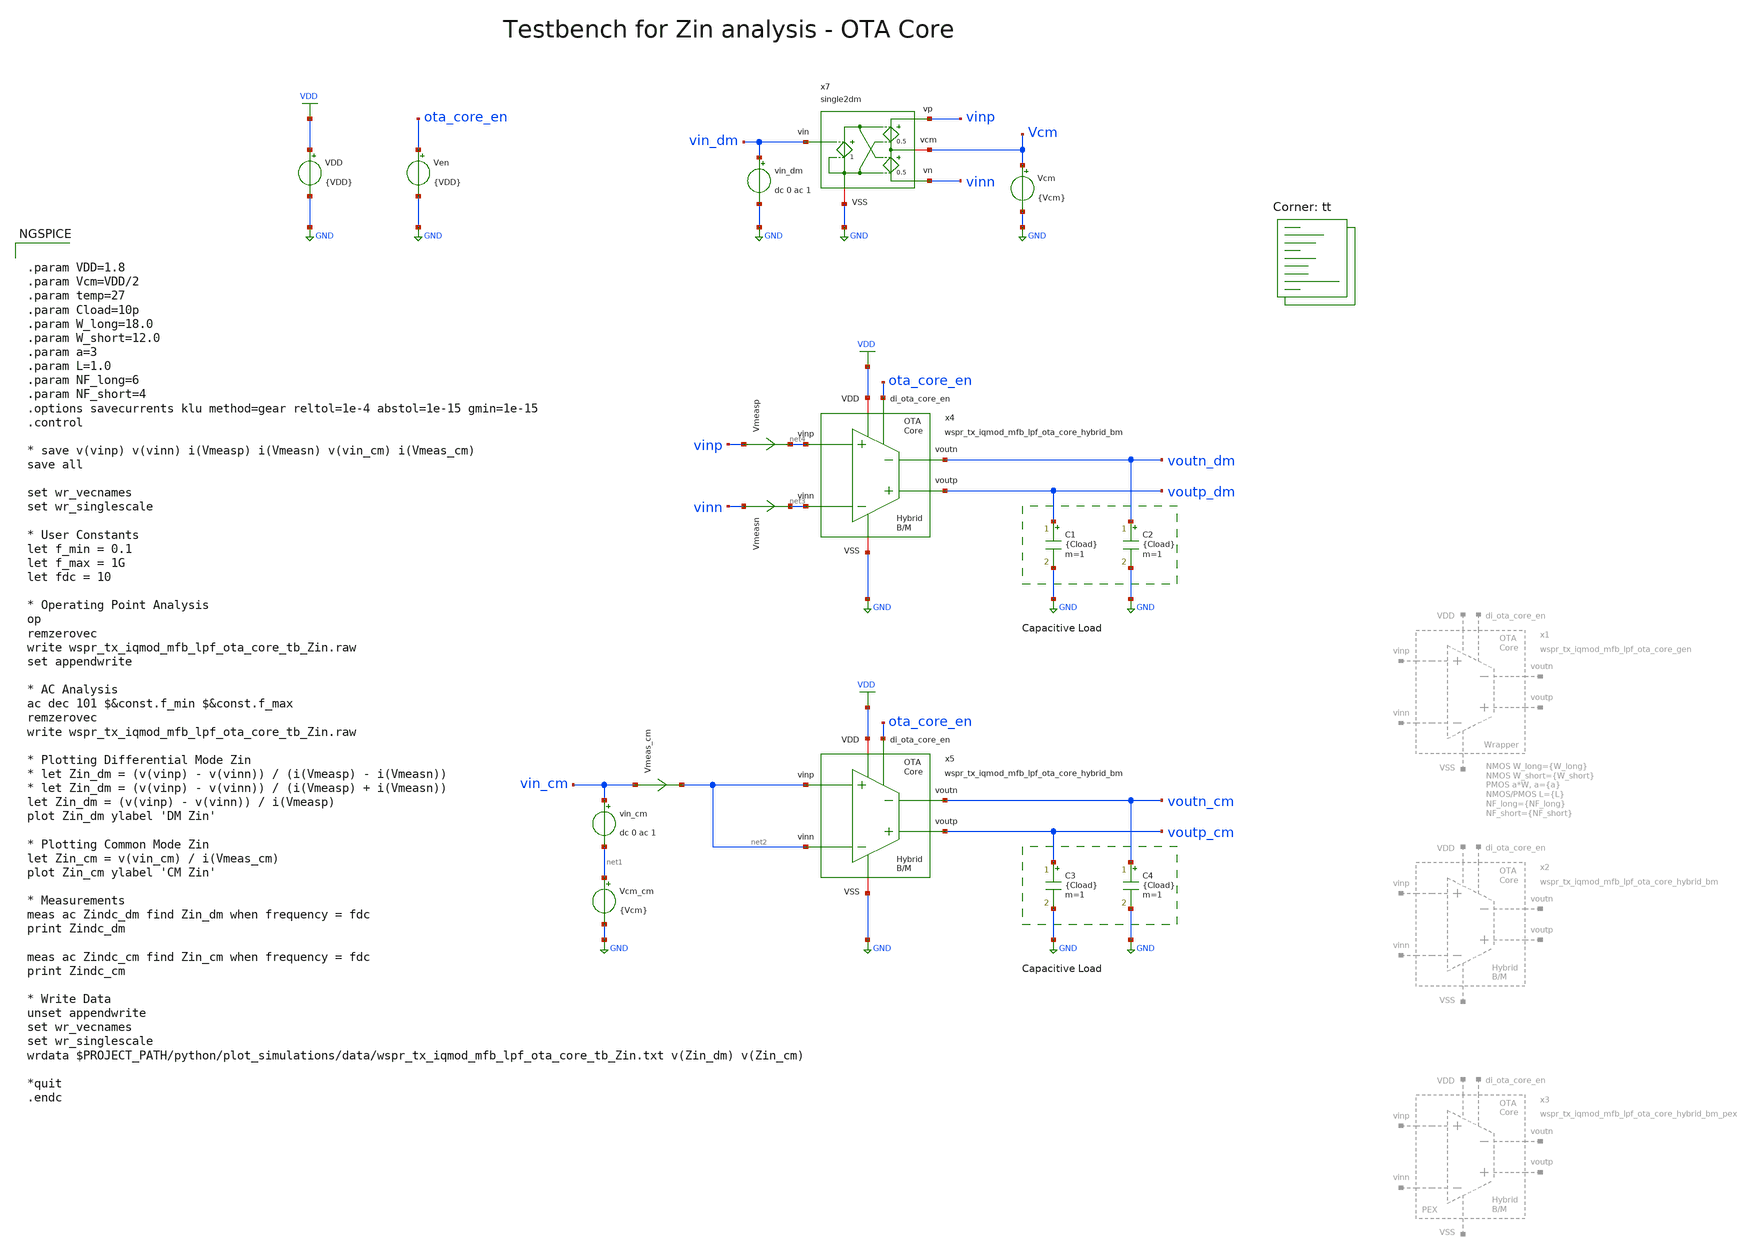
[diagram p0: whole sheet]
** sch_path: sky130/macros/iqmod/testbenches/wspr_tx_iqmod_mfb_lpf_ota_core_tb_Zin.sch
**.subckt wspr_tx_iqmod_mfb_lpf_ota_core_tb_Zin
VDD VDD GND {VDD}
C1 voutp_dm GND {Cload} m=1
C2 voutn_dm GND {Cload} m=1
Ven ota_core_en GND {VDD}
C3 voutp_cm GND {Cload} m=1
C4 voutn_cm GND {Cload} m=1
vin_cm vin_cm net1 dc 0 ac 1
Vmeasp vinp net4 0
.save i(vmeasp)
Vmeasn vinn net3 0
.save i(vmeasn)
Vmeas_cm vin_cm net2 0
.save i(vmeas_cm)
Vcm_cm net1 GND {Vcm}
vin_dm vin_dm GND dc 0 ac 1
x4 ota_core_en voutp_dm voutn_dm net3 net4 VDD GND wspr_tx_iqmod_mfb_lpf_ota_core_hybrid_bm
x5 ota_core_en voutp_cm voutn_cm net2 net2 VDD GND wspr_tx_iqmod_mfb_lpf_ota_core_hybrid_bm
x7 vinp vin_dm Vcm GND vinn single2dm
Vcm Vcm GND {Vcm}
**** begin user architecture code


.param VDD=1.8
.param Vcm=VDD/2
.param temp=27
.param Cload=10p
.param W_long=18.0
.param W_short=12.0
.param a=3
.param L=1.0
.param NF_long=6
.param NF_short=4
.options savecurrents klu method=gear reltol=1e-4 abstol=1e-15 gmin=1e-15
.control

* save v(vinp) v(vinn) i(Vmeasp) i(Vmeasn) v(vin_cm) i(Vmeas_cm)
save all

set wr_vecnames
set wr_singlescale

* User Constants
let f_min = 0.1
let f_max = 1G
let fdc = 10

* Operating Point Analysis
op
remzerovec
write wspr_tx_iqmod_mfb_lpf_ota_core_tb_Zin.raw
set appendwrite

* AC Analysis
ac dec 101 $&const.f_min $&const.f_max
remzerovec
write wspr_tx_iqmod_mfb_lpf_ota_core_tb_Zin.raw

* Plotting Differential Mode Zin
* let Zin_dm = (v(vinp) - v(vinn)) / (i(Vmeasp) - i(Vmeasn))
* let Zin_dm = (v(vinp) - v(vinn)) / (i(Vmeasp) + i(Vmeasn))
let Zin_dm = (v(vinp) - v(vinn)) / i(Vmeasp)
plot Zin_dm ylabel 'DM Zin'

* Plotting Common Mode Zin
let Zin_cm = v(vin_cm) / i(Vmeas_cm)
plot Zin_cm ylabel 'CM Zin'

* Measurements
meas ac Zindc_dm find Zin_dm when frequency = fdc
print Zindc_dm

meas ac Zindc_cm find Zin_cm when frequency = fdc
print Zindc_cm

* Write Data
unset appendwrite
set wr_vecnames
set wr_singlescale
wrdata $PROJECT_PATH/python/plot_simulations/data/wspr_tx_iqmod_mfb_lpf_ota_core_tb_Zin.txt
+ v(Zin_dm) v(Zin_cm)

*quit
.endc


.lib $::SKYWATER_MODELS/sky130.lib.spice tt
**** end user architecture code
**.ends
.GLOBAL GND
.GLOBAL VDD
.end
